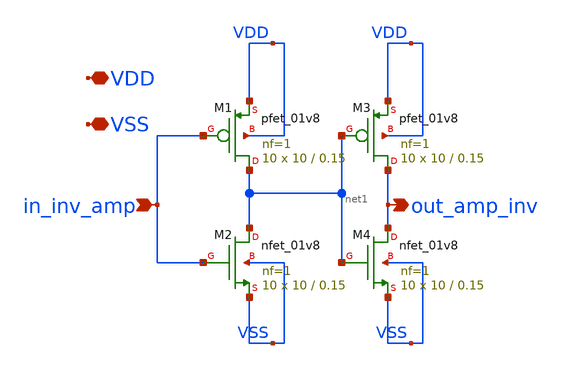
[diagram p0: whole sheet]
** sch_path: xschem/double_inverter.sch
**.subckt double_inverter VDD VSS in_inv_amp out_amp_inv
*.iopin VDD
*.iopin VSS
*.ipin in_inv_amp
*.opin out_amp_inv
XM1 net1 in_inv_amp VDD VDD sky130_fd_pr__pfet_01v8 L=0.15 W=10 nf=1 ad='int((nf+1)/2) * W/nf * 0.29'
+ as='int((nf+2)/2) * W/nf * 0.29' pd='2*int((nf+1)/2) * (W/nf + 0.29)' ps='2*int((nf+2)/2) * (W/nf + 0.29)'
+ nrd='0.29 / W' nrs='0.29 / W' sa=0 sb=0 sd=0 mult=10 m=10
XM2 net1 in_inv_amp VSS VSS sky130_fd_pr__nfet_01v8 L=0.15 W=10 nf=1 ad='int((nf+1)/2) * W/nf * 0.29'
+ as='int((nf+2)/2) * W/nf * 0.29' pd='2*int((nf+1)/2) * (W/nf + 0.29)' ps='2*int((nf+2)/2) * (W/nf + 0.29)'
+ nrd='0.29 / W' nrs='0.29 / W' sa=0 sb=0 sd=0 mult=10 m=10
XM3 out_amp_inv net1 VDD VDD sky130_fd_pr__pfet_01v8 L=0.15 W=10 nf=1 ad='int((nf+1)/2) * W/nf * 0.29'
+ as='int((nf+2)/2) * W/nf * 0.29' pd='2*int((nf+1)/2) * (W/nf + 0.29)' ps='2*int((nf+2)/2) * (W/nf + 0.29)'
+ nrd='0.29 / W' nrs='0.29 / W' sa=0 sb=0 sd=0 mult=10 m=10
XM4 out_amp_inv net1 VSS VSS sky130_fd_pr__nfet_01v8 L=0.15 W=10 nf=1 ad='int((nf+1)/2) * W/nf * 0.29'
+ as='int((nf+2)/2) * W/nf * 0.29' pd='2*int((nf+1)/2) * (W/nf + 0.29)' ps='2*int((nf+2)/2) * (W/nf + 0.29)'
+ nrd='0.29 / W' nrs='0.29 / W' sa=0 sb=0 sd=0 mult=10 m=10
**.ends
.end
